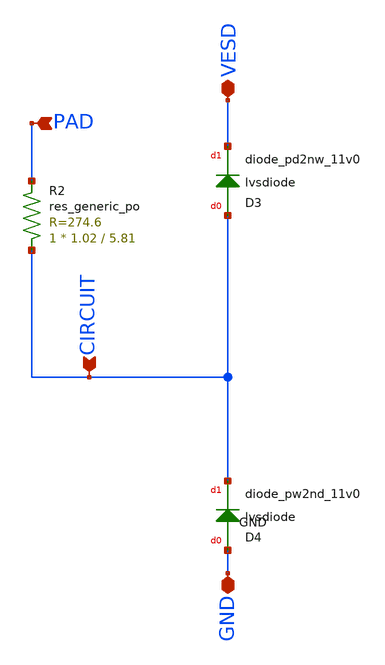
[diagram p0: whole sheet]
** sch_path: sky130_cells/ESD_Diode/ESD_Flatten_Pins.sch
**.subckt ESD_Flatten_Pins GND VESD CIRCUIT PAD
*.iopin GND
*.iopin VESD
*.ipin CIRCUIT
*.ipin PAD
D3 CIRCUIT VESD sky130_fd_pr__diode_pd2nw_11v0 area=4.40146e13
D4 GND CIRCUIT sky130_fd_pr__diode_pw2nd_11v0 area=2.59996e13
XR2 CIRCUIT PAD sky130_fd_pr__res_generic_po W=1.02 L=5.81 m=1
**.ends
.end
